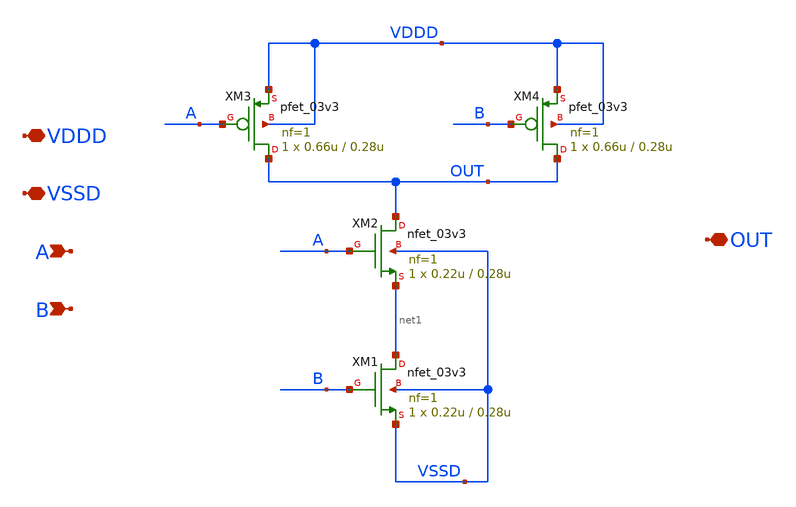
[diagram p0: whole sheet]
** sch_path: SAR_ADC/blocks/Dynamic_Comparator/Dynamic_Comparator_nand_1x.sch
**.subckt Dynamic_Comparator_nand_1x VDDD VSSD A B OUT
*.iopin VDDD
*.iopin VSSD
*.ipin A
*.ipin B
*.iopin OUT
XM1 net1 B VSSD VSSD nfet_03v3 L=0.28u W=0.22u nf=1 ad='int((nf+1)/2) * W/nf * 0.18u' as='int((nf+2)/2) * W/nf * 0.18u'
+ pd='2*int((nf+1)/2) * (W/nf + 0.18u)' ps='2*int((nf+2)/2) * (W/nf + 0.18u)' nrd='0.18u / W' nrs='0.18u / W'
+ sa=0 sb=0 sd=0 m=1
XM2 OUT A net1 VSSD nfet_03v3 L=0.28u W=0.22u nf=1 ad='int((nf+1)/2) * W/nf * 0.18u' as='int((nf+2)/2) * W/nf * 0.18u'
+ pd='2*int((nf+1)/2) * (W/nf + 0.18u)' ps='2*int((nf+2)/2) * (W/nf + 0.18u)' nrd='0.18u / W' nrs='0.18u / W'
+ sa=0 sb=0 sd=0 m=1
XM3 OUT A VDDD VDDD pfet_03v3 L=0.28u W=0.66u nf=1 ad='int((nf+1)/2) * W/nf * 0.18u' as='int((nf+2)/2) * W/nf * 0.18u'
+ pd='2*int((nf+1)/2) * (W/nf + 0.18u)' ps='2*int((nf+2)/2) * (W/nf + 0.18u)' nrd='0.18u / W' nrs='0.18u / W'
+ sa=0 sb=0 sd=0 m=1
XM4 OUT B VDDD VDDD pfet_03v3 L=0.28u W=0.66u nf=1 ad='int((nf+1)/2) * W/nf * 0.18u' as='int((nf+2)/2) * W/nf * 0.18u'
+ pd='2*int((nf+1)/2) * (W/nf + 0.18u)' ps='2*int((nf+2)/2) * (W/nf + 0.18u)' nrd='0.18u / W' nrs='0.18u / W'
+ sa=0 sb=0 sd=0 m=1
**.ends
.end
